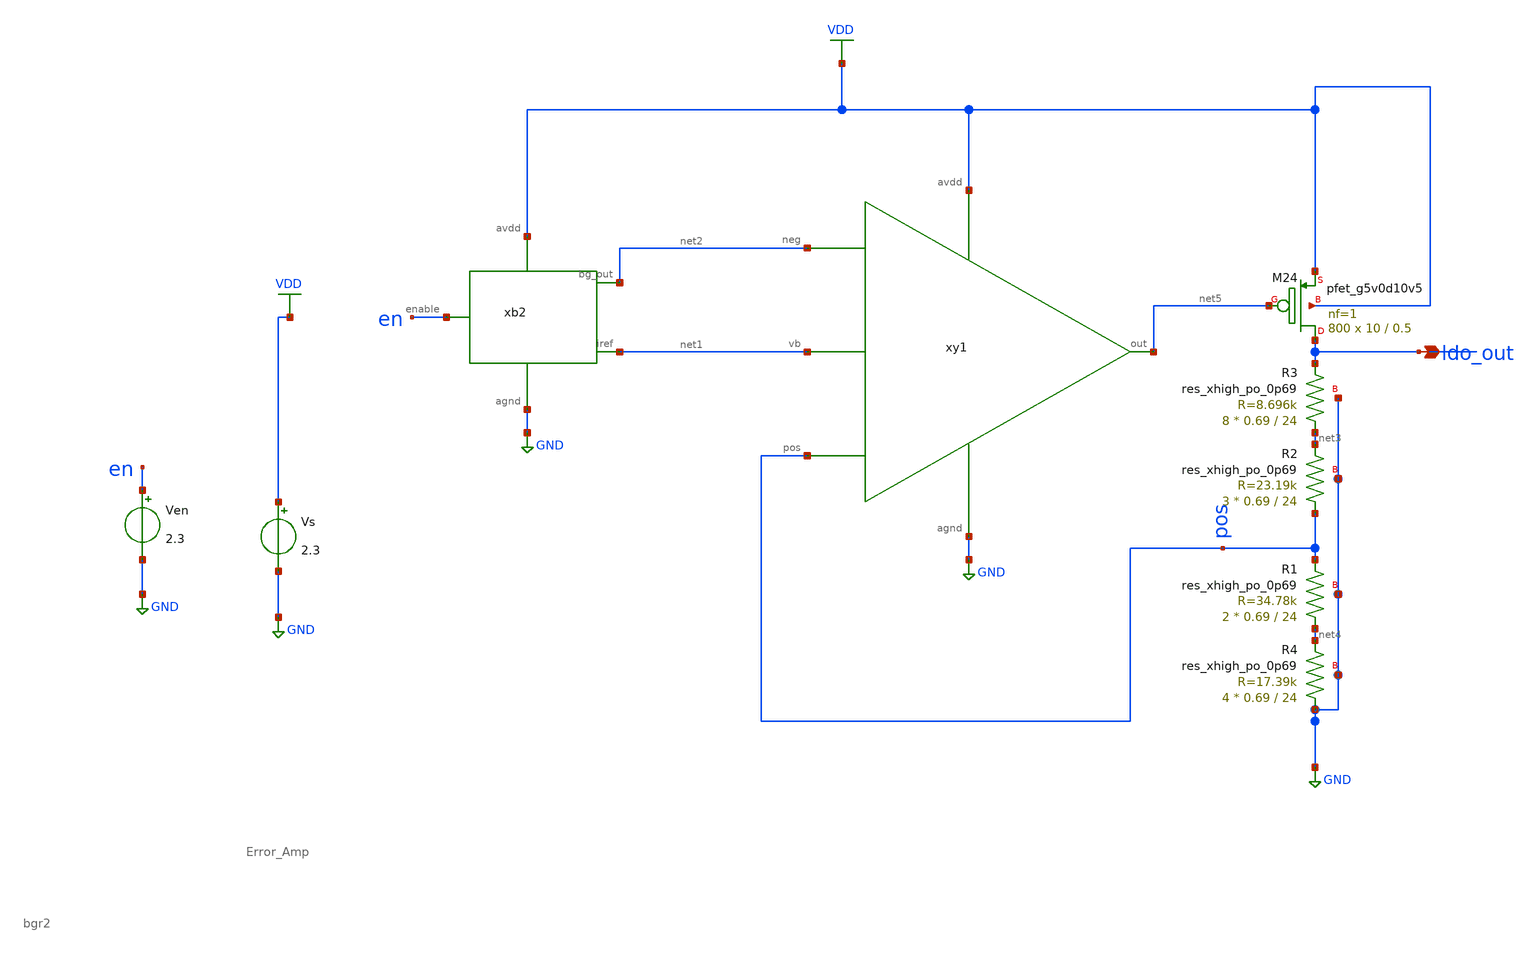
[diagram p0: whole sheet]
** sch_path: xschem/ldo_v2/ldo_v2_sim.sch
**.subckt ldo_v2_sim ldo_out
*.opin ldo_out
xb2 net2 net1 GND VDD en bgr2
xy1 net2 pos net1 net5 VDD GND Error_Amp
XM24 ldo_out net5 VDD VDD sky130_fd_pr__pfet_g5v0d10v5 L=0.5 W=10 nf=1 ad='int((nf+1)/2) * W/nf * 0.29'
+ as='int((nf+2)/2) * W/nf * 0.29' pd='2*int((nf+1)/2) * (W/nf + 0.29)' ps='2*int((nf+2)/2) * (W/nf + 0.29)'
+ nrd='0.29 / W' nrs='0.29 / W' sa=0 sb=0 sd=0 mult=800 m=800
XR2 pos net3 GND sky130_fd_pr__res_xhigh_po_0p69 L=24 mult=3 m=3
XR3 net3 ldo_out GND sky130_fd_pr__res_xhigh_po_0p69 L=24 mult=8 m=8
XR1 net4 pos GND sky130_fd_pr__res_xhigh_po_0p69 L=24 mult=2 m=2
XR4 GND net4 GND sky130_fd_pr__res_xhigh_po_0p69 L=24 mult=4 m=4
Vs VDD GND 2.3
Ven en GND 2.3
**** begin user architecture code



.param R=36k
R10 ldo_out GND {R}
IL ldo_out 0 PWL(0 0.1m 10u 0.1m 20u 10m 30u 10m)
*CL ldo_out gnd 10p
.lib /home/mustafa/mabrains/pdks/share/pdk/sky130A/libs.tech/ngspice/sky130.lib_mod.spice tt





.nodeset v(x1.inn)=1.2
.nodeset v(x1.inp)=1.2
.nodeset v(x1.mir)=1
.nodeset v(x1.net5)=1
.nodeset v(x1.bg_out)=1.1
.nodeset v(ldo_out)=1.8
.nodeset v(pos)=1.1
*.nodeset v(net3)=0.8
*.nodeset v(net1)=0.7
.nodeset v(x1.net6)=0.9
*.nodeset v(net7)=0.75
.nodeset v(xy1.vb)=0.9


.option temp=27
*User_defined_functions
.control
define max(vector_name) (vecmax(vector_name))
define min(vector_name) (vecmin(vector_name))
.endc


*Temp_sweep
.control
alter IL 0
dc temp 85 0 -1
let temp_coeff=1000000*(max(ldo_out)-min(ldo_out))/85
print temp_coeff
plot v(ldo_out)
set wr_singlescale
set wr_vecnames
set appendwrite
.endc


.control
alter IL 0
*alter R10 1G
op
let iq =i(Vs)
print iq
*print all
set wr_singlescale
set wr_vecnames
set appendwrite
if v(ldo_out)>1
wrdata op_point_test v(ldo_out)
end
.endc



*Stability_Analysis
.control
alter IL 0
alter Vs AC =0
alter Vt AC=1
ac dec 10 1 1G
plot vdb(out)
plot (180/pi)*vp(out)
let ph= (180/pi)*vp(out)
meas ac pm FIND ph WHEN vdb(out)=0
.endc


*PSRR_Analysis
.control
alter IL 0
alter Vs AC =1
alter Vt AC=0
alter L1 0
alter C2 0
ac dec 10 1 1G
meas AC PSRR100 FIND vdb(ldo_out) AT=100
meas AC PSRR100k FIND vdb(ldo_out) AT=100k
plot vdb(ldo_out)
.endc




*supply_sweep
.control
alter IL 0
dc Vs 2.8 0 -0.01
plot vdd ldo_out
meas DC Vldo_Sup_2 FIND ldo_out AT=2
meas DC Vldo_nom FIND ldo_out AT=2.3
meas DC Vldo_Sup_2_8 FIND ldo_out AT=2.8
let line_reg = abs((Vldo_Sup_2_8-Vldo_Sup_2)/0.8)
print line_reg
meas DC vin WHEN v(ldo_out)=1.764
let dropout=vin-1.764
print dropout
set wr_singlescale
set wr_vecnames
set appendwrite
.endc





*Load_Reg_switches
*V1 c1 0 DC 0 PWL(0 5 20u 5 35u 0 50u 0 100u 0)
*V2 c2 0 DC 0 PWL(0 0 20u 0 35u 0 50u 5 100u 5)
*s1 ldo_out 2 c1 0 switch1 ON
*s2 ldo_out 3 c2 0 switch1 OFF
*.model switch1 sw vt=0.1 ron =0.1 roff =1G
*R1 2 0 18k
*R2 3 0 180

*.control
*alter R10 1G
*tran 0.1u 90u
*plot v(ldo_out) v(c1) v(c2)
*meas TRAN V_ldo_100u FIND v(ldo_out) AT=10u
*meas TRAN V_ldo_10m FIND v(ldo_out) AT=50u
*let load_reg= V_ldo_100u-V_ldo_10m
*print load_reg
*.endc


**Load_Transient
.control
alter IL 50u
alter R10 3600k
tran 0.1u 100u
meas TRAN V_ldo_100u FIND v(ldo_out) AT=5u
meas TRAN V_ldo_10m FIND v(ldo_out) AT=100u
let load_reg= V_ldo_100u-V_ldo_10m
let load_current =(-1*i(Vs)-131.8e-6)
print load_reg
plot load_current v(ldo_out)-1.8
.endc


**Transient
.control
alter R10 36k
alter @IL[PWL] = [ 0 0 10u 0 20u 0 30u 0 ]
alter @Vs[pulse] = [ 1.8 3 10u 10u 1u 100u 200u ]
alter IL 0
tran 0.1u 100u
plot vdd ldo_out
.endc
.control
alter R10 36k
alter @IL[PWL] = [ 0 0 10u 0 20u 0 30u 0 ]
alter @Vs[pulse] = [ 0 2.3 10u 0.1u 1u 100u 200u ]
tran 0.1u 100u
plot vdd ldo_out
.endc
.control
alter R10 36k
alter @IL[PWL] = [ 0 0 10u 0 20u 0 30u 0 ]
alter @Ven[pulse] = [ 0 2.3 10u 0.1u 1u 100u 200u ]
tran 0.1u 100u
*meas TRAN st_up_time when v(ldo_out)>1.782
plot en ldo_out
.endc







**** end user architecture code
**.ends

* expanding   symbol:  ldo_v2/bgr2.sym # of pins=5
** sym_path: xschem/ldo_v2/bgr2.sym
** sch_path: xschem/ldo_v2/bgr2.sch
.subckt bgr2 bg_out iref agnd avdd enable
*.ipin avdd
*.ipin agnd
*.opin bg_out
*.ipin enable
*.ipin iref
XM1 inn mir avdd avdd sky130_fd_pr__pfet_g5v0d10v5 L=2 W=3 nf=1 ad='int((nf+1)/2) * W/nf * 0.29' as='int((nf+2)/2) * W/nf * 0.29'
+ pd='2*int((nf+1)/2) * (W/nf + 0.29)' ps='2*int((nf+2)/2) * (W/nf + 0.29)' nrd='0.29 / W' nrs='0.29 / W'
+ sa=0 sb=0 sd=0 mult=8 m=8
XM2 inp mir avdd avdd sky130_fd_pr__pfet_g5v0d10v5 L=2 W=3 nf=1 ad='int((nf+1)/2) * W/nf * 0.29' as='int((nf+2)/2) * W/nf * 0.29'
+ pd='2*int((nf+1)/2) * (W/nf + 0.29)' ps='2*int((nf+2)/2) * (W/nf + 0.29)' nrd='0.29 / W' nrs='0.29 / W'
+ sa=0 sb=0 sd=0 mult=8 m=8
XM3 bg_out mir avdd avdd sky130_fd_pr__pfet_g5v0d10v5 L=2 W=3 nf=1 ad='int((nf+1)/2) * W/nf * 0.29' as='int((nf+2)/2) * W/nf * 0.29'
+ pd='2*int((nf+1)/2) * (W/nf + 0.29)' ps='2*int((nf+2)/2) * (W/nf + 0.29)' nrd='0.29 / W' nrs='0.29 / W'
+ sa=0 sb=0 sd=0 mult=8 m=8
XQ1 agnd agnd net2 sky130_fd_pr__pnp_05v5_W0p68L0p68 m=1
XQ5 agnd agnd net1 sky130_fd_pr__pnp_05v5_W0p68L0p68 m=1
XQ6 agnd agnd net1 sky130_fd_pr__pnp_05v5_W0p68L0p68 m=1
XQ7 agnd agnd net1 sky130_fd_pr__pnp_05v5_W0p68L0p68 m=1
XQ9 agnd agnd net1 sky130_fd_pr__pnp_05v5_W0p68L0p68 m=1
XQ11 agnd agnd net1 sky130_fd_pr__pnp_05v5_W0p68L0p68 m=1
XQ13 agnd agnd net1 sky130_fd_pr__pnp_05v5_W0p68L0p68 m=1
XQ15 agnd agnd net1 sky130_fd_pr__pnp_05v5_W0p68L0p68 m=1
XQ17 agnd agnd net1 sky130_fd_pr__pnp_05v5_W0p68L0p68 m=1
XM7 net4 net4 avdd avdd sky130_fd_pr__pfet_g5v0d10v5 L=2 W=3 nf=1 ad='int((nf+1)/2) * W/nf * 0.29' as='int((nf+2)/2) * W/nf * 0.29'
+ pd='2*int((nf+1)/2) * (W/nf + 0.29)' ps='2*int((nf+2)/2) * (W/nf + 0.29)' nrd='0.29 / W' nrs='0.29 / W'
+ sa=0 sb=0 sd=0 mult=4 m=4
XM12 net4 inp net3 agnd sky130_fd_pr__nfet_g5v0d10v5 L=1 W=3 nf=1 ad='int((nf+1)/2) * W/nf * 0.29' as='int((nf+2)/2) * W/nf * 0.29'
+ pd='2*int((nf+1)/2) * (W/nf + 0.29)' ps='2*int((nf+2)/2) * (W/nf + 0.29)' nrd='0.29 / W' nrs='0.29 / W'
+ sa=0 sb=0 sd=0 mult=8 m=8
XM21 mir inn net3 agnd sky130_fd_pr__nfet_g5v0d10v5 L=1 W=3 nf=1 ad='int((nf+1)/2) * W/nf * 0.29' as='int((nf+2)/2) * W/nf * 0.29'
+ pd='2*int((nf+1)/2) * (W/nf + 0.29)' ps='2*int((nf+2)/2) * (W/nf + 0.29)' nrd='0.29 / W' nrs='0.29 / W'
+ sa=0 sb=0 sd=0 mult=8 m=8
XM23 mir net4 avdd avdd sky130_fd_pr__pfet_g5v0d10v5 L=2 W=3 nf=1 ad='int((nf+1)/2) * W/nf * 0.29' as='int((nf+2)/2) * W/nf * 0.29'
+ pd='2*int((nf+1)/2) * (W/nf + 0.29)' ps='2*int((nf+2)/2) * (W/nf + 0.29)' nrd='0.29 / W' nrs='0.29 / W'
+ sa=0 sb=0 sd=0 mult=4 m=4
XM15 net3 net5 agnd agnd sky130_fd_pr__nfet_g5v0d10v5 L=2 W=5 nf=1 ad='int((nf+1)/2) * W/nf * 0.29' as='int((nf+2)/2) * W/nf * 0.29'
+ pd='2*int((nf+1)/2) * (W/nf + 0.29)' ps='2*int((nf+2)/2) * (W/nf + 0.29)' nrd='0.29 / W' nrs='0.29 / W'
+ sa=0 sb=0 sd=0 mult=4 m=4
XM25 net5 mir avdd avdd sky130_fd_pr__pfet_g5v0d10v5 L=2 W=3 nf=1 ad='int((nf+1)/2) * W/nf * 0.29' as='int((nf+2)/2) * W/nf * 0.29'
+ pd='2*int((nf+1)/2) * (W/nf + 0.29)' ps='2*int((nf+2)/2) * (W/nf + 0.29)' nrd='0.29 / W' nrs='0.29 / W'
+ sa=0 sb=0 sd=0 mult=8 m=8
XM16 net5 net5 agnd agnd sky130_fd_pr__nfet_g5v0d10v5 L=2 W=5 nf=1 ad='int((nf+1)/2) * W/nf * 0.29' as='int((nf+2)/2) * W/nf * 0.29'
+ pd='2*int((nf+1)/2) * (W/nf + 0.29)' ps='2*int((nf+2)/2) * (W/nf + 0.29)' nrd='0.29 / W' nrs='0.29 / W'
+ sa=0 sb=0 sd=0 mult=4 m=4
XC1 mir agnd sky130_fd_pr__cap_mim_m3_1 W=16 L=16 MF=1 m=1
XR1 net6 inp agnd sky130_fd_pr__res_xhigh_po_0p69 L=27 mult=3 m=3
XR2 net2 inn agnd sky130_fd_pr__res_xhigh_po_0p69 L=27 mult=3 m=3
XR3 net8 net2 agnd sky130_fd_pr__res_xhigh_po_0p69 L=27 mult=1 m=1
XR10 net1 net6 agnd sky130_fd_pr__res_xhigh_po_0p69 L=27 mult=6 m=6
XR4 agnd net7 agnd sky130_fd_pr__res_xhigh_po_0p69 L=27 mult=15 m=15
XR11 agnd net8 agnd sky130_fd_pr__res_xhigh_po_0p69 L=27 mult=15 m=15
XR6 net7 net6 agnd sky130_fd_pr__res_xhigh_po_0p69 L=27 mult=1 m=1
XR5 net9 bg_out agnd sky130_fd_pr__res_xhigh_po_0p69 L=27 mult=1 m=1
XR14 agnd net9 agnd sky130_fd_pr__res_xhigh_po_0p69 L=27 mult=53 m=53
XM19 mir enable avdd avdd sky130_fd_pr__pfet_g5v0d10v5 L=0.5 W=0.42 nf=1 ad='int((nf+1)/2) * W/nf * 0.29'
+ as='int((nf+2)/2) * W/nf * 0.29' pd='2*int((nf+1)/2) * (W/nf + 0.29)' ps='2*int((nf+2)/2) * (W/nf + 0.29)'
+ nrd='0.29 / W' nrs='0.29 / W' sa=0 sb=0 sd=0 mult=2 m=2
XM4 net10 bg_out avdd avdd sky130_fd_pr__pfet_g5v0d10v5 L=5 W=0.42 nf=1 ad='int((nf+1)/2) * W/nf * 0.29'
+ as='int((nf+2)/2) * W/nf * 0.29' pd='2*int((nf+1)/2) * (W/nf + 0.29)' ps='2*int((nf+2)/2) * (W/nf + 0.29)'
+ nrd='0.29 / W' nrs='0.29 / W' sa=0 sb=0 sd=0 mult=2 m=2
XM5 net10 bg_out agnd agnd sky130_fd_pr__nfet_g5v0d10v5 L=0.5 W=10 nf=1 ad='int((nf+1)/2) * W/nf * 0.29'
+ as='int((nf+2)/2) * W/nf * 0.29' pd='2*int((nf+1)/2) * (W/nf + 0.29)' ps='2*int((nf+2)/2) * (W/nf + 0.29)'
+ nrd='0.29 / W' nrs='0.29 / W' sa=0 sb=0 sd=0 mult=8 m=8
XM6 avdd net10 inn agnd sky130_fd_pr__nfet_g5v0d10v5 L=0.5 W=3 nf=1 ad='int((nf+1)/2) * W/nf * 0.29'
+ as='int((nf+2)/2) * W/nf * 0.29' pd='2*int((nf+1)/2) * (W/nf + 0.29)' ps='2*int((nf+2)/2) * (W/nf + 0.29)'
+ nrd='0.29 / W' nrs='0.29 / W' sa=0 sb=0 sd=0 mult=4 m=4
XM26 iref mir avdd avdd sky130_fd_pr__pfet_g5v0d10v5 L=2 W=3 nf=1 ad='int((nf+1)/2) * W/nf * 0.29' as='int((nf+2)/2) * W/nf * 0.29'
+ pd='2*int((nf+1)/2) * (W/nf + 0.29)' ps='2*int((nf+2)/2) * (W/nf + 0.29)' nrd='0.29 / W' nrs='0.29 / W'
+ sa=0 sb=0 sd=0 mult=4 m=4
.ends


* expanding   symbol:  ldo_v1/Error_Amp.sym # of pins=6
** sym_path: xschem/ldo_v1/Error_Amp.sym
** sch_path: xschem/ldo_v1/Error_Amp.sch
.subckt Error_Amp neg pos vb out avdd agnd
*.opin out
*.iopin avdd
*.iopin agnd
*.iopin vb
*.ipin neg
*.ipin pos
XM8 net2 net2 avdd avdd sky130_fd_pr__pfet_g5v0d10v5 L=1.2 W=3 nf=1 ad='int((nf+1)/2) * W/nf * 0.29'
+ as='int((nf+2)/2) * W/nf * 0.29' pd='2*int((nf+1)/2) * (W/nf + 0.29)' ps='2*int((nf+2)/2) * (W/nf + 0.29)'
+ nrd='0.29 / W' nrs='0.29 / W' sa=0 sb=0 sd=0 mult=4 m=4
XM9 net2 neg net3 agnd sky130_fd_pr__nfet_g5v0d10v5 L=1 W=2 nf=1 ad='int((nf+1)/2) * W/nf * 0.29' as='int((nf+2)/2) * W/nf * 0.29'
+ pd='2*int((nf+1)/2) * (W/nf + 0.29)' ps='2*int((nf+2)/2) * (W/nf + 0.29)' nrd='0.29 / W' nrs='0.29 / W'
+ sa=0 sb=0 sd=0 mult=8 m=8
XM10 net1 pos net3 agnd sky130_fd_pr__nfet_g5v0d10v5 L=1 W=2 nf=1 ad='int((nf+1)/2) * W/nf * 0.29' as='int((nf+2)/2) * W/nf * 0.29'
+ pd='2*int((nf+1)/2) * (W/nf + 0.29)' ps='2*int((nf+2)/2) * (W/nf + 0.29)' nrd='0.29 / W' nrs='0.29 / W'
+ sa=0 sb=0 sd=0 mult=8 m=8
XM11 net1 net2 avdd avdd sky130_fd_pr__pfet_g5v0d10v5 L=1.2 W=3 nf=1 ad='int((nf+1)/2) * W/nf * 0.29'
+ as='int((nf+2)/2) * W/nf * 0.29' pd='2*int((nf+1)/2) * (W/nf + 0.29)' ps='2*int((nf+2)/2) * (W/nf + 0.29)'
+ nrd='0.29 / W' nrs='0.29 / W' sa=0 sb=0 sd=0 mult=4 m=4
XM13 net3 vb agnd agnd sky130_fd_pr__nfet_g5v0d10v5 L=1 W=1 nf=1 ad='int((nf+1)/2) * W/nf * 0.29' as='int((nf+2)/2) * W/nf * 0.29'
+ pd='2*int((nf+1)/2) * (W/nf + 0.29)' ps='2*int((nf+2)/2) * (W/nf + 0.29)' nrd='0.29 / W' nrs='0.29 / W'
+ sa=0 sb=0 sd=0 mult=8 m=8
XM14 out net1 avdd avdd sky130_fd_pr__pfet_g5v0d10v5 L=1.2 W=3 nf=1 ad='int((nf+1)/2) * W/nf * 0.29'
+ as='int((nf+2)/2) * W/nf * 0.29' pd='2*int((nf+1)/2) * (W/nf + 0.29)' ps='2*int((nf+2)/2) * (W/nf + 0.29)'
+ nrd='0.29 / W' nrs='0.29 / W' sa=0 sb=0 sd=0 mult=12 m=12
XM18 out vb agnd agnd sky130_fd_pr__nfet_g5v0d10v5 L=1 W=1 nf=1 ad='int((nf+1)/2) * W/nf * 0.29' as='int((nf+2)/2) * W/nf * 0.29'
+ pd='2*int((nf+1)/2) * (W/nf + 0.29)' ps='2*int((nf+2)/2) * (W/nf + 0.29)' nrd='0.29 / W' nrs='0.29 / W'
+ sa=0 sb=0 sd=0 mult=12 m=12
XC3 net1 net4 sky130_fd_pr__cap_mim_m3_1 W=50 L=50 MF=1 m=1
XR7 out net4 agnd sky130_fd_pr__res_xhigh_po_0p69 L=4.5 mult=1 m=1
XM20 vb vb agnd agnd sky130_fd_pr__nfet_g5v0d10v5 L=1 W=1 nf=1 ad='int((nf+1)/2) * W/nf * 0.29' as='int((nf+2)/2) * W/nf * 0.29'
+ pd='2*int((nf+1)/2) * (W/nf + 0.29)' ps='2*int((nf+2)/2) * (W/nf + 0.29)' nrd='0.29 / W' nrs='0.29 / W'
+ sa=0 sb=0 sd=0 mult=4 m=4
.ends

.GLOBAL GND
.GLOBAL VDD
.end
